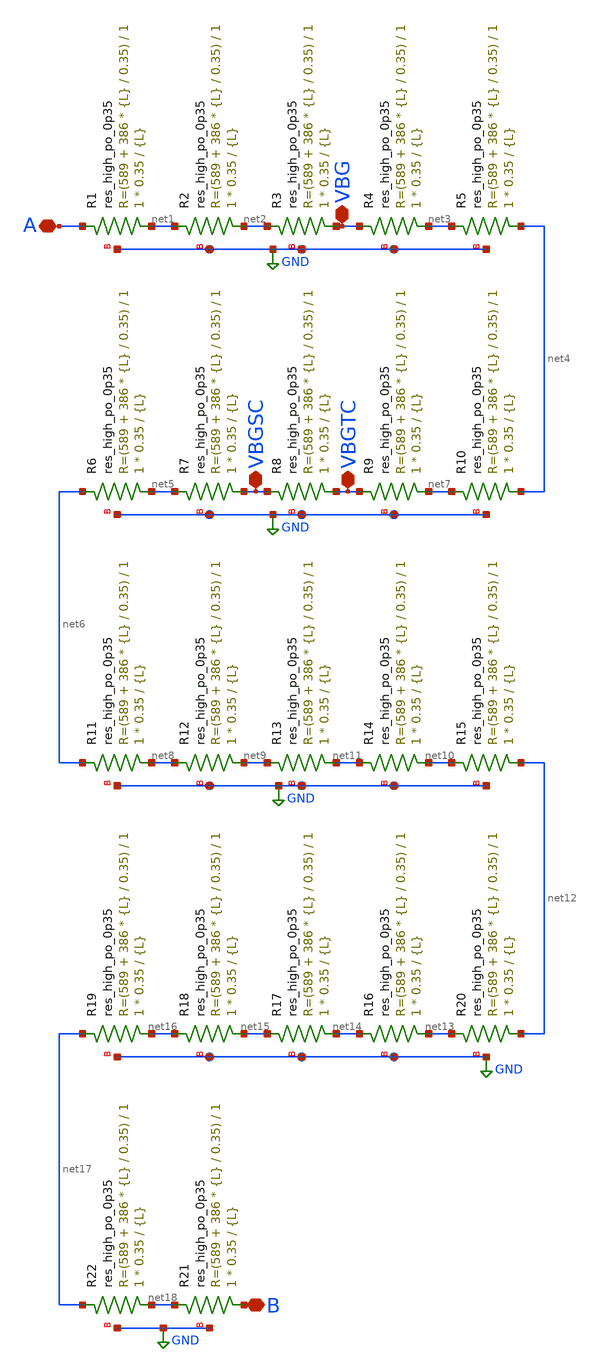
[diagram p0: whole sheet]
** sch_path: xschem/Resistor492k_exp.sch
**.subckt Resistor492k_exp A VBGTC B VBGSC VBG
*.iopin A
*.iopin VBGTC
*.iopin B
*.iopin VBGSC
*.iopin VBG
XR1 net1 A GND sky130_fd_pr__res_high_po_0p35 L={L} mult=1 m=1
XR2 net2 net1 GND sky130_fd_pr__res_high_po_0p35 L={L} mult=1 m=1
XR3 VBG net2 GND sky130_fd_pr__res_high_po_0p35 L={L} mult=1 m=1
XR4 net3 VBG GND sky130_fd_pr__res_high_po_0p35 L={L} mult=1 m=1
XR5 net4 net3 GND sky130_fd_pr__res_high_po_0p35 L={L} mult=1 m=1
XR6 net5 net6 GND sky130_fd_pr__res_high_po_0p35 L={L} mult=1 m=1
XR7 VBGSC net5 GND sky130_fd_pr__res_high_po_0p35 L={L} mult=1 m=1
XR8 VBGTC VBGSC GND sky130_fd_pr__res_high_po_0p35 L={L} mult=1 m=1
XR9 net7 VBGTC GND sky130_fd_pr__res_high_po_0p35 L={L} mult=1 m=1
XR10 net4 net7 GND sky130_fd_pr__res_high_po_0p35 L={L} mult=1 m=1
XR11 net8 net6 GND sky130_fd_pr__res_high_po_0p35 L={L} mult=1 m=1
XR12 net9 net8 GND sky130_fd_pr__res_high_po_0p35 L={L} mult=1 m=1
XR13 net11 net9 GND sky130_fd_pr__res_high_po_0p35 L={L} mult=1 m=1
XR14 net10 net11 GND sky130_fd_pr__res_high_po_0p35 L={L} mult=1 m=1
XR15 net12 net10 GND sky130_fd_pr__res_high_po_0p35 L={L} mult=1 m=1
XR20 net12 net13 GND sky130_fd_pr__res_high_po_0p35 L={L} mult=1 m=1
XR16 net13 net14 GND sky130_fd_pr__res_high_po_0p35 L={L} mult=1 m=1
XR17 net14 net15 GND sky130_fd_pr__res_high_po_0p35 L={L} mult=1 m=1
XR18 net15 net16 GND sky130_fd_pr__res_high_po_0p35 L={L} mult=1 m=1
XR19 net16 net17 GND sky130_fd_pr__res_high_po_0p35 L={L} mult=1 m=1
XR21 B net18 GND sky130_fd_pr__res_high_po_0p35 L={L} mult=1 m=1
XR22 net18 net17 GND sky130_fd_pr__res_high_po_0p35 L={L} mult=1 m=1
**** begin user architecture code


.param L=17


**** end user architecture code
**.ends
.GLOBAL GND
.end
